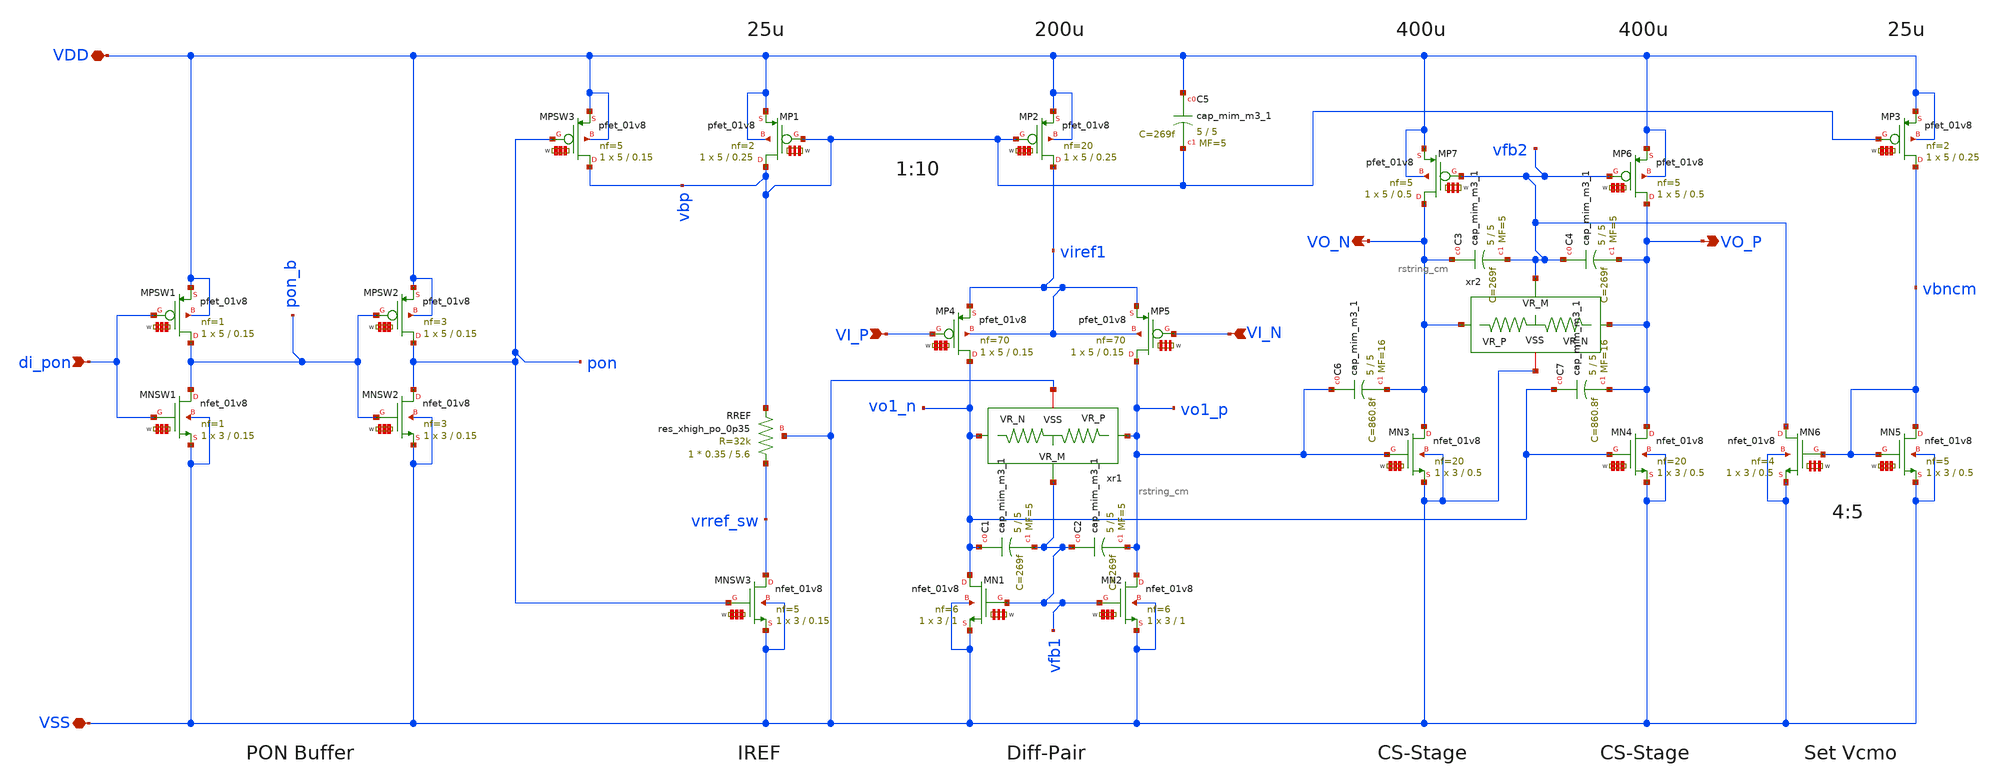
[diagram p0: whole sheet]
** sch_path: xschem/amp.sch
**.subckt amp VSS VDD VI_P di_pon VI_N VO_P VO_N
*.iopin VSS
*.iopin VDD
*.ipin VI_P
*.ipin di_pon
*.ipin VI_N
*.opin VO_P
*.opin VO_N
XMP1 vbp vbp VDD VDD sky130_fd_pr__pfet_01v8 L=0.25 W='5 * 2 ' nf=2 ad='int((nf+1)/2) * W / nf * 0.29'
+ as='int((nf+2)/2) * W / nf * 0.29' pd='2*int((nf+1)/2) * (W / nf + 0.29)' ps='2*int((nf+2)/2) * (W / nf + 0.29)'
+ nrd='0.29 / W ' nrs='0.29 / W ' sa=0 sb=0 sd=0 mult=1 m=1
XMPSW3 vbp pon VDD VDD sky130_fd_pr__pfet_01v8 L=0.15 W='5 * 5 ' nf=5 ad='int((nf+1)/2) * W / nf * 0.29'
+ as='int((nf+2)/2) * W / nf * 0.29' pd='2*int((nf+1)/2) * (W / nf + 0.29)' ps='2*int((nf+2)/2) * (W / nf + 0.29)'
+ nrd='0.29 / W ' nrs='0.29 / W ' sa=0 sb=0 sd=0 mult=1 m=1
XMNSW1 pon_b di_pon VSS VSS sky130_fd_pr__nfet_01v8 L=0.15 W='3 * 1 ' nf=1 ad='int((nf+1)/2) * W / nf * 0.29'
+ as='int((nf+2)/2) * W / nf * 0.29' pd='2*int((nf+1)/2) * (W / nf + 0.29)' ps='2*int((nf+2)/2) * (W / nf + 0.29)'
+ nrd='0.29 / W ' nrs='0.29 / W ' sa=0 sb=0 sd=0 mult=1 m=1
XMPSW1 pon_b di_pon VDD VDD sky130_fd_pr__pfet_01v8 L=0.15 W='5 * 1 ' nf=1 ad='int((nf+1)/2) * W / nf * 0.29'
+ as='int((nf+2)/2) * W / nf * 0.29' pd='2*int((nf+1)/2) * (W / nf + 0.29)' ps='2*int((nf+2)/2) * (W / nf + 0.29)'
+ nrd='0.29 / W ' nrs='0.29 / W ' sa=0 sb=0 sd=0 mult=1 m=1
XMNSW2 pon pon_b VSS VSS sky130_fd_pr__nfet_01v8 L=0.15 W='3 * 3 ' nf=3 ad='int((nf+1)/2) * W / nf * 0.29'
+ as='int((nf+2)/2) * W / nf * 0.29' pd='2*int((nf+1)/2) * (W / nf + 0.29)' ps='2*int((nf+2)/2) * (W / nf + 0.29)'
+ nrd='0.29 / W ' nrs='0.29 / W ' sa=0 sb=0 sd=0 mult=1 m=1
XMPSW2 pon pon_b VDD VDD sky130_fd_pr__pfet_01v8 L=0.15 W='5 * 3 ' nf=3 ad='int((nf+1)/2) * W / nf * 0.29'
+ as='int((nf+2)/2) * W / nf * 0.29' pd='2*int((nf+1)/2) * (W / nf + 0.29)' ps='2*int((nf+2)/2) * (W / nf + 0.29)'
+ nrd='0.29 / W ' nrs='0.29 / W ' sa=0 sb=0 sd=0 mult=1 m=1
XMP2 viref1 vbp VDD VDD sky130_fd_pr__pfet_01v8 L=0.25 W='5 * 20 ' nf=20 ad='int((nf+1)/2) * W / nf * 0.29'
+ as='int((nf+2)/2) * W / nf * 0.29' pd='2*int((nf+1)/2) * (W / nf + 0.29)' ps='2*int((nf+2)/2) * (W / nf + 0.29)'
+ nrd='0.29 / W ' nrs='0.29 / W ' sa=0 sb=0 sd=0 mult=1 m=1
XC5 VDD vbp sky130_fd_pr__cap_mim_m3_1 W=5 L=5 MF=5 m=5
XMP4 vo1_n VI_P viref1 viref1 sky130_fd_pr__pfet_01v8 L=0.15 W='5 * 70 ' nf=70 ad='int((nf+1)/2) * W / nf * 0.29'
+ as='int((nf+2)/2) * W / nf * 0.29' pd='2*int((nf+1)/2) * (W / nf + 0.29)' ps='2*int((nf+2)/2) * (W / nf + 0.29)'
+ nrd='0.29 / W ' nrs='0.29 / W ' sa=0 sb=0 sd=0 mult=1 m=1
XMP5 vo1_p VI_N viref1 viref1 sky130_fd_pr__pfet_01v8 L=0.15 W='5 * 70 ' nf=70 ad='int((nf+1)/2) * W / nf * 0.29'
+ as='int((nf+2)/2) * W / nf * 0.29' pd='2*int((nf+1)/2) * (W / nf + 0.29)' ps='2*int((nf+2)/2) * (W / nf + 0.29)'
+ nrd='0.29 / W ' nrs='0.29 / W ' sa=0 sb=0 sd=0 mult=1 m=1
XMN1 vo1_n vfb1 VSS VSS sky130_fd_pr__nfet_01v8 L=1 W='3 * 6 ' nf=6 ad='int((nf+1)/2) * W / nf * 0.29'
+ as='int((nf+2)/2) * W / nf * 0.29' pd='2*int((nf+1)/2) * (W / nf + 0.29)' ps='2*int((nf+2)/2) * (W / nf + 0.29)'
+ nrd='0.29 / W ' nrs='0.29 / W ' sa=0 sb=0 sd=0 mult=1 m=1
XMN2 vo1_p vfb1 VSS VSS sky130_fd_pr__nfet_01v8 L=1 W='3 * 6 ' nf=6 ad='int((nf+1)/2) * W / nf * 0.29'
+ as='int((nf+2)/2) * W / nf * 0.29' pd='2*int((nf+1)/2) * (W / nf + 0.29)' ps='2*int((nf+2)/2) * (W / nf + 0.29)'
+ nrd='0.29 / W ' nrs='0.29 / W ' sa=0 sb=0 sd=0 mult=1 m=1
XC1 vo1_n vfb1 sky130_fd_pr__cap_mim_m3_1 W=5 L=5 MF=5 m=5
XC2 vfb1 vo1_p sky130_fd_pr__cap_mim_m3_1 W=5 L=5 MF=5 m=5
XMN3 VO_N vo1_p VSS VSS sky130_fd_pr__nfet_01v8 L=0.5 W='3 * 20 ' nf=20 ad='int((nf+1)/2) * W / nf * 0.29'
+ as='int((nf+2)/2) * W / nf * 0.29' pd='2*int((nf+1)/2) * (W / nf + 0.29)' ps='2*int((nf+2)/2) * (W / nf + 0.29)'
+ nrd='0.29 / W ' nrs='0.29 / W ' sa=0 sb=0 sd=0 mult=1 m=1
XMN4 VO_P vo1_n VSS VSS sky130_fd_pr__nfet_01v8 L=0.5 W='3 * 20 ' nf=20 ad='int((nf+1)/2) * W / nf * 0.29'
+ as='int((nf+2)/2) * W / nf * 0.29' pd='2*int((nf+1)/2) * (W / nf + 0.29)' ps='2*int((nf+2)/2) * (W / nf + 0.29)'
+ nrd='0.29 / W ' nrs='0.29 / W ' sa=0 sb=0 sd=0 mult=1 m=1
XMP3 vbncm vbp VDD VDD sky130_fd_pr__pfet_01v8 L=0.25 W='5 * 2 ' nf=2 ad='int((nf+1)/2) * W / nf * 0.29'
+ as='int((nf+2)/2) * W / nf * 0.29' pd='2*int((nf+1)/2) * (W / nf + 0.29)' ps='2*int((nf+2)/2) * (W / nf + 0.29)'
+ nrd='0.29 / W ' nrs='0.29 / W ' sa=0 sb=0 sd=0 mult=1 m=1
XMP6 VO_P vfb2 VDD VDD sky130_fd_pr__pfet_01v8 L=0.5 W='5 * 5 ' nf=5 ad='int((nf+1)/2) * W / nf * 0.29'
+ as='int((nf+2)/2) * W / nf * 0.29' pd='2*int((nf+1)/2) * (W / nf + 0.29)' ps='2*int((nf+2)/2) * (W / nf + 0.29)'
+ nrd='0.29 / W ' nrs='0.29 / W ' sa=0 sb=0 sd=0 mult=1 m=1
XMP7 VO_N vfb2 VDD VDD sky130_fd_pr__pfet_01v8 L=0.5 W='5 * 5 ' nf=5 ad='int((nf+1)/2) * W / nf * 0.29'
+ as='int((nf+2)/2) * W / nf * 0.29' pd='2*int((nf+1)/2) * (W / nf + 0.29)' ps='2*int((nf+2)/2) * (W / nf + 0.29)'
+ nrd='0.29 / W ' nrs='0.29 / W ' sa=0 sb=0 sd=0 mult=1 m=1
XC3 VO_N vfb2 sky130_fd_pr__cap_mim_m3_1 W=5 L=5 MF=5 m=5
XC4 vfb2 VO_P sky130_fd_pr__cap_mim_m3_1 W=5 L=5 MF=5 m=5
XMN5 vbncm vbncm VSS VSS sky130_fd_pr__nfet_01v8 L=0.5 W='3 * 5 ' nf=5 ad='int((nf+1)/2) * W / nf * 0.29'
+ as='int((nf+2)/2) * W / nf * 0.29' pd='2*int((nf+1)/2) * (W / nf + 0.29)' ps='2*int((nf+2)/2) * (W / nf + 0.29)'
+ nrd='0.29 / W ' nrs='0.29 / W ' sa=0 sb=0 sd=0 mult=1 m=1
XMN6 vfb2 vbncm VSS VSS sky130_fd_pr__nfet_01v8 L=0.5 W='3 * 4 ' nf=4 ad='int((nf+1)/2) * W / nf * 0.29'
+ as='int((nf+2)/2) * W / nf * 0.29' pd='2*int((nf+1)/2) * (W / nf + 0.29)' ps='2*int((nf+2)/2) * (W / nf + 0.29)'
+ nrd='0.29 / W ' nrs='0.29 / W ' sa=0 sb=0 sd=0 mult=1 m=1
XMNSW3 vrref_sw pon VSS VSS sky130_fd_pr__nfet_01v8 L=0.15 W='3 * 5 ' nf=5 ad='int((nf+1)/2) * W / nf * 0.29'
+ as='int((nf+2)/2) * W / nf * 0.29' pd='2*int((nf+1)/2) * (W / nf + 0.29)' ps='2*int((nf+2)/2) * (W / nf + 0.29)'
+ nrd='0.29 / W ' nrs='0.29 / W ' sa=0 sb=0 sd=0 mult=1 m=1
XRREF vrref_sw vbp VSS sky130_fd_pr__res_xhigh_po_0p35 L=5.6 mult=1 m=1
xr1 vfb1 vo1_n vo1_p VSS rstring_cm
xr2 vfb2 VO_P VO_N VSS rstring_cm
XC6 vo1_p VO_N sky130_fd_pr__cap_mim_m3_1 W=5 L=5 MF=16 m=16
XC7 vo1_n VO_P sky130_fd_pr__cap_mim_m3_1 W=5 L=5 MF=16 m=16
**.ends

* expanding   symbol:  /foss/designs/xschem/rstring_cm.sym # of pins=4
** sym_path: xschem/rstring_cm.sym
** sch_path: xschem/rstring_cm.sch
.subckt rstring_cm VR_M VR_N VR_P VSS
*.iopin VSS
*.ipin VR_P
*.ipin VR_N
*.opin VR_M
XR1 VR_P net1 VSS sky130_fd_pr__res_xhigh_po_0p35 L=5.6 mult=1 m=1
XR2 net1 VR_M VSS sky130_fd_pr__res_xhigh_po_0p35 L=5.6 mult=1 m=1
XR3 VR_M net2 VSS sky130_fd_pr__res_xhigh_po_0p35 L=5.6 mult=1 m=1
XR4 net2 VR_N VSS sky130_fd_pr__res_xhigh_po_0p35 L=5.6 mult=1 m=1
.ends

.end
